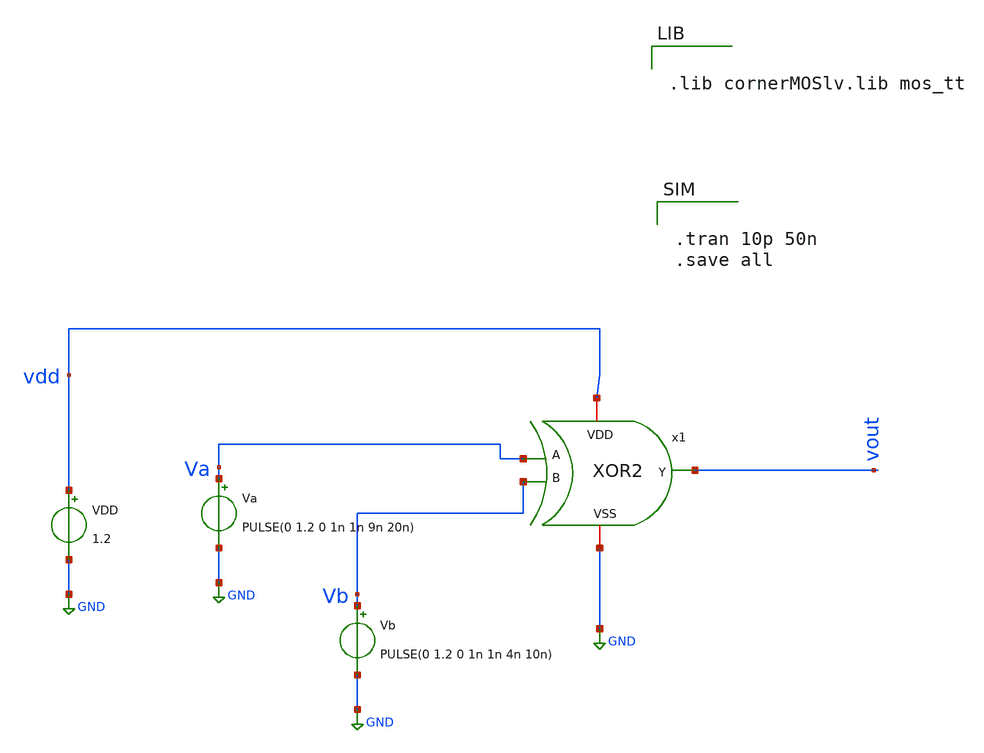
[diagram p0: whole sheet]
** sch_path: TestXOR.sch
**.subckt TestXOR
Va Va GND PULSE(0 1.2 0 1n 1n 9n 20n)
VDD vdd GND 1.2
Vb Vb GND PULSE(0 1.2 0 1n 1n 4n 10n)
x1 vdd Va vout Vb GND XOR2
**** begin user architecture code


.lib cornerMOSlv.lib mos_tt




.tran 10p 50n
.save all


**** end user architecture code
**.ends

* expanding   symbol:  /foss/designs/LogicGate/XOR2.sym # of pins=5
** sym_path: LogicGate/XOR2.sym
** sch_path: LogicGate/XOR2.sch
.subckt XOR2 VDD A Y B VSS
*.opin Y
*.iopin VSS
*.iopin VDD
*.ipin A
*.ipin B
XM1 net3 A' VDD VDD sg13_lv_pmos w=0.15u l=0.13u ng=1 m=1 mm_ok=1
XM2 Y B net3 VDD sg13_lv_pmos w=0.15u l=0.13u ng=1 m=1 mm_ok=1
XM3 net4 A VDD VDD sg13_lv_pmos w=0.15u l=0.13u ng=1 m=1 mm_ok=1
XM4 Y B' net4 VDD sg13_lv_pmos w=0.15u l=0.13u ng=1 m=1 mm_ok=1
XM5 Y A net1 VSS sg13_lv_nmos w=0.15u l=0.13u ng=1 m=1 mm_ok=1
XM6 net1 B VSS VSS sg13_lv_nmos w=0.15u l=0.13u ng=1 m=1 mm_ok=1
XM7 Y A' net2 VSS sg13_lv_nmos w=0.15u l=0.13u ng=1 m=1 mm_ok=1
XM8 net2 B' VSS VSS sg13_lv_nmos w=0.15u l=0.13u ng=1 m=1 mm_ok=1
x1 VDD A A' VSS inverter
x2 VDD B B' VSS inverter
.ends


* expanding   symbol:  /foss/designs/BTDay6-Ex/inverter.sym # of pins=4
** sym_path: BTDay6-Ex/inverter.sym
** sch_path: BTDay6-Ex/inverter.sch
.subckt inverter VDD A Y VSS
*.ipin A
*.opin Y
*.iopin VDD
*.iopin VSS
XM1 Y A VSS VSS sg13_lv_nmos w=0.15u l=0.13u ng=1 m=1 mm_ok=1
XM2 Y A VDD VDD sg13_lv_pmos w=0.15u l=0.13u ng=1 m=1 mm_ok=1
.ends

.GLOBAL GND
.end
